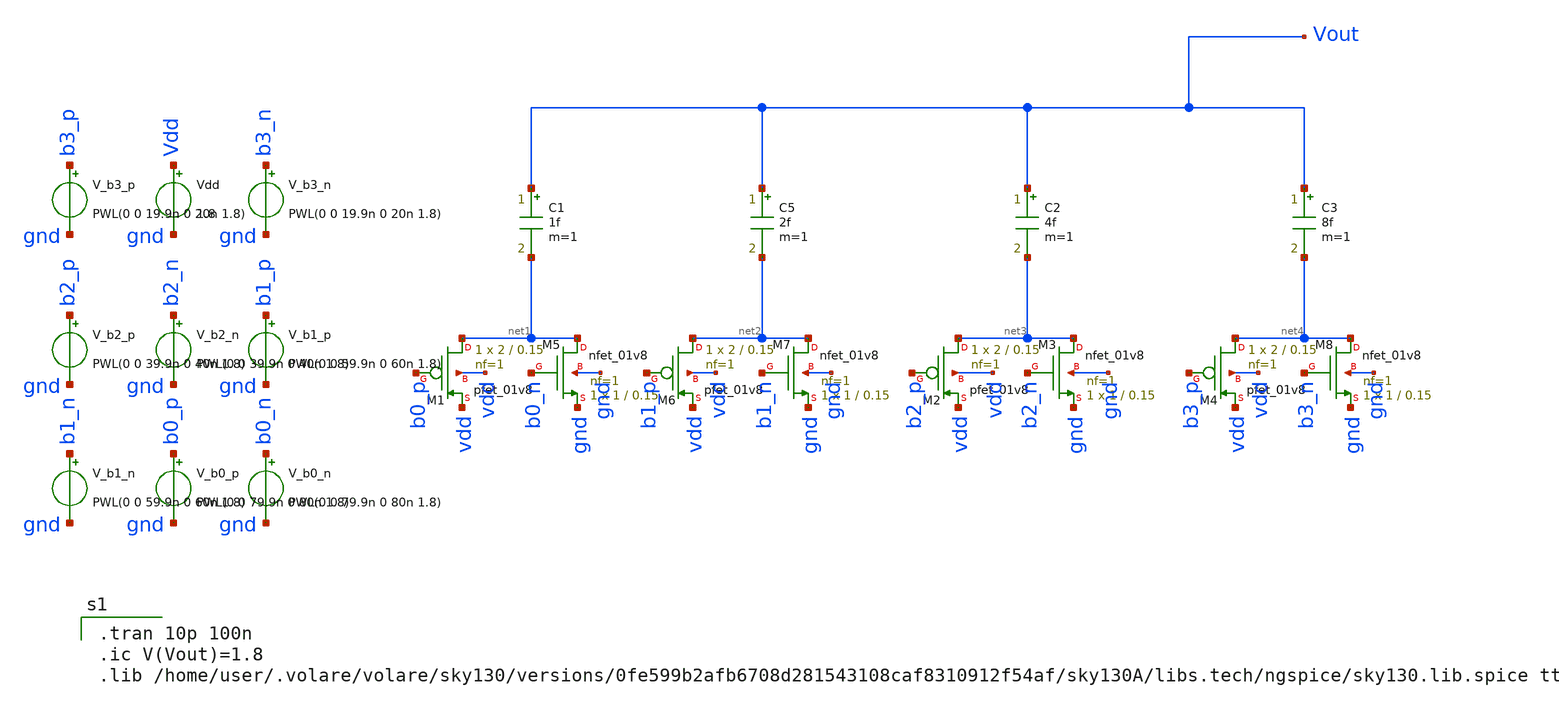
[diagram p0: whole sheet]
** sch_path: sar_adc_dac_monotonic/monotonic_dac.sch
**.subckt monotonic_dac
C1 Vout net1 1f m=1
XM1 net1 b0_p vdd vdd sky130_fd_pr__pfet_01v8 L=0.15 W=2 nf=1 ad='int((nf+1)/2) * W/nf * 0.29' as='int((nf+2)/2) * W/nf * 0.29'
+ pd='2*int((nf+1)/2) * (W/nf + 0.29)' ps='2*int((nf+2)/2) * (W/nf + 0.29)' nrd='0.29 / W' nrs='0.29 / W'
+ sa=0 sb=0 sd=0 mult=1 m=1
XM5 net1 b0_n gnd gnd sky130_fd_pr__nfet_01v8 L=0.15 W=1 nf=1 ad='int((nf+1)/2) * W/nf * 0.29' as='int((nf+2)/2) * W/nf * 0.29'
+ pd='2*int((nf+1)/2) * (W/nf + 0.29)' ps='2*int((nf+2)/2) * (W/nf + 0.29)' nrd='0.29 / W' nrs='0.29 / W'
+ sa=0 sb=0 sd=0 mult=1 m=1
C5 Vout net2 2f m=1
XM6 net2 b1_p vdd vdd sky130_fd_pr__pfet_01v8 L=0.15 W=2 nf=1 ad='int((nf+1)/2) * W/nf * 0.29' as='int((nf+2)/2) * W/nf * 0.29'
+ pd='2*int((nf+1)/2) * (W/nf + 0.29)' ps='2*int((nf+2)/2) * (W/nf + 0.29)' nrd='0.29 / W' nrs='0.29 / W'
+ sa=0 sb=0 sd=0 mult=1 m=1
XM7 net2 b1_n gnd gnd sky130_fd_pr__nfet_01v8 L=0.15 W=1 nf=1 ad='int((nf+1)/2) * W/nf * 0.29' as='int((nf+2)/2) * W/nf * 0.29'
+ pd='2*int((nf+1)/2) * (W/nf + 0.29)' ps='2*int((nf+2)/2) * (W/nf + 0.29)' nrd='0.29 / W' nrs='0.29 / W'
+ sa=0 sb=0 sd=0 mult=1 m=1
C2 Vout net3 4f m=1
XM2 net3 b2_p vdd vdd sky130_fd_pr__pfet_01v8 L=0.15 W=2 nf=1 ad='int((nf+1)/2) * W/nf * 0.29' as='int((nf+2)/2) * W/nf * 0.29'
+ pd='2*int((nf+1)/2) * (W/nf + 0.29)' ps='2*int((nf+2)/2) * (W/nf + 0.29)' nrd='0.29 / W' nrs='0.29 / W'
+ sa=0 sb=0 sd=0 mult=1 m=1
XM3 net3 b2_n gnd gnd sky130_fd_pr__nfet_01v8 L=0.15 W=1 nf=1 ad='int((nf+1)/2) * W/nf * 0.29' as='int((nf+2)/2) * W/nf * 0.29'
+ pd='2*int((nf+1)/2) * (W/nf + 0.29)' ps='2*int((nf+2)/2) * (W/nf + 0.29)' nrd='0.29 / W' nrs='0.29 / W'
+ sa=0 sb=0 sd=0 mult=1 m=1
C3 Vout net4 8f m=1
XM4 net4 b3_p vdd vdd sky130_fd_pr__pfet_01v8 L=0.15 W=2 nf=1 ad='int((nf+1)/2) * W/nf * 0.29' as='int((nf+2)/2) * W/nf * 0.29'
+ pd='2*int((nf+1)/2) * (W/nf + 0.29)' ps='2*int((nf+2)/2) * (W/nf + 0.29)' nrd='0.29 / W' nrs='0.29 / W'
+ sa=0 sb=0 sd=0 mult=1 m=1
XM8 net4 b3_n gnd gnd sky130_fd_pr__nfet_01v8 L=0.15 W=1 nf=1 ad='int((nf+1)/2) * W/nf * 0.29' as='int((nf+2)/2) * W/nf * 0.29'
+ pd='2*int((nf+1)/2) * (W/nf + 0.29)' ps='2*int((nf+2)/2) * (W/nf + 0.29)' nrd='0.29 / W' nrs='0.29 / W'
+ sa=0 sb=0 sd=0 mult=1 m=1
Vdd Vdd gnd 1.8
V_b3_p b3_p gnd PWL(0 0 19.9n 0 20n 1.8)
V_b3_n b3_n gnd PWL(0 0 19.9n 0 20n 1.8)
V_b2_p b2_p gnd PWL(0 0 39.9n 0 40n 1.8)
V_b2_n b2_n gnd PWL(0 0 39.9n 0 40n 1.8)
V_b1_p b1_p gnd PWL(0 0 59.9n 0 60n 1.8)
V_b1_n b1_n gnd PWL(0 0 59.9n 0 60n 1.8)
V_b0_p b0_p gnd PWL(0 0 79.9n 0 80n 1.8)
V_b0_n b0_n gnd PWL(0 0 79.9n 0 80n 1.8)
**** begin user architecture code

.tran 10p 100n
.ic V(Vout)=1.8
.lib /home/user/.volare/volare/sky130/versions/0fe599b2afb6708d281543108caf8310912f54af/sky130A/libs.tech/ngspice/sky130.lib.spice tt

**** end user architecture code
**.ends
.end
